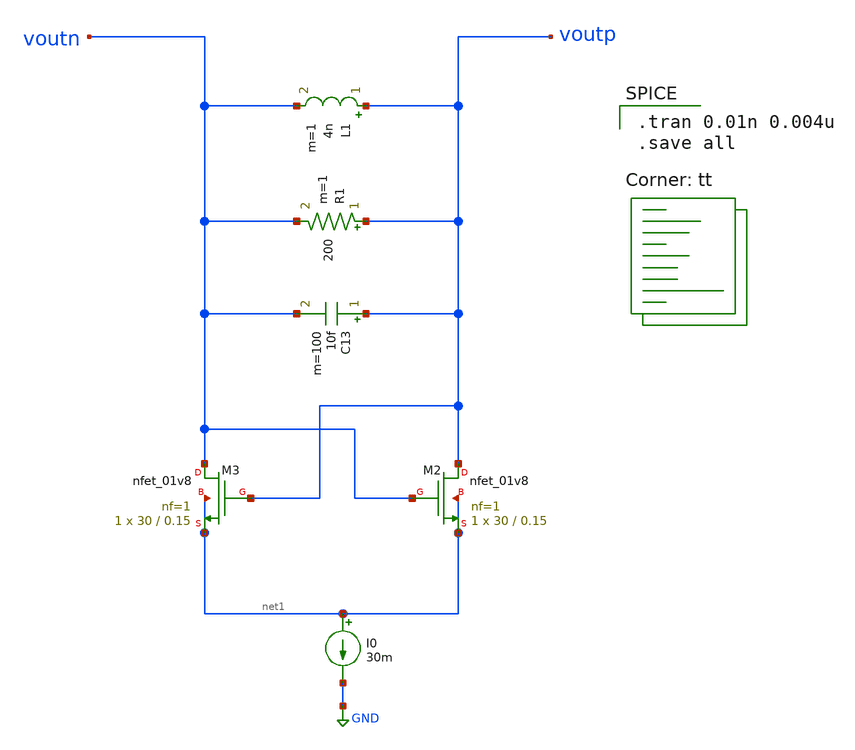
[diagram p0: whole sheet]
** sch_path: pll/lc_vco_lib_Ahmed_Reda/VCO_NMOS_init_tb/xschem/VCO_NMOS_init_tb.sch
**.subckt VCO_NMOS_init_tb
XM2 voutp voutn net1 net1 sky130_fd_pr__nfet_01v8 L=0.15 W=30 nf=1 ad='int((1 + 1)/2) * 30 / 1 * 0.29'
+ as='int((1 + 2)/2) * 30 / 1 * 0.29' pd='2*int((1 + 1)/2) * (30 / 1 + 0.29)' ps='2*int((1 + 2)/2) * (30 / 1 + 0.29)'
+ nrd='0.29 / 30 ' nrs='0.29 / 30 ' sa=0 sb=0 sd=0 mult=1 m=1
XM3 voutn voutp net1 net1 sky130_fd_pr__nfet_01v8 L=0.15 W=30 nf=1 ad='int((1 + 1)/2) * 30 / 1 * 0.29'
+ as='int((1 + 2)/2) * 30 / 1 * 0.29' pd='2*int((1 + 1)/2) * (30 / 1 + 0.29)' ps='2*int((1 + 2)/2) * (30 / 1 + 0.29)'
+ nrd='0.29 / 30 ' nrs='0.29 / 30 ' sa=0 sb=0 sd=0 mult=1 m=1
L1 voutp voutn 4n m=1
I0 net1 GND 30m
C13 voutp voutn 10f m=100
R1 voutp voutn 200 m=1
**** begin user architecture code
.lib $::SKYWATER_MODELS/sky130.lib.spice tt

.tran 0.01n 0.004u
.save all


** opencircuitdesign pdks install
.lib $::SKYWATER_MODELS/sky130.lib.spice tt


**** end user architecture code
**.ends
.GLOBAL GND
.end
